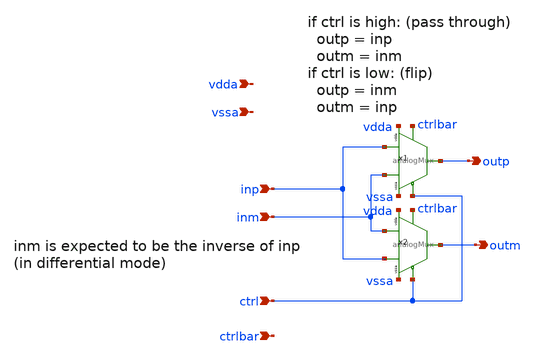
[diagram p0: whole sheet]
** sch_path: xschem/archive/mux/multiplier_differential.sch
**.subckt multiplier_differential inp inm outp outm ctrl ctrlbar vdda vssa
*.ipin inp
*.ipin inm
*.opin outp
*.opin outm
*.ipin ctrl
*.ipin ctrlbar
*.ipin vdda
*.ipin vssa
x1 inm inp ctrlbar ctrl outp vssa vdda analogMux
x2 inp inm ctrlbar ctrl outm vssa vdda analogMux
**.ends

* expanding   symbol:  mux/analogMux.sym # of pins=7
** sym_path: xschem/mux/analogMux.sym
** sch_path: xschem/mux/analogMux.sch
.subckt analogMux vref2 vref1 c cbar out vssa vdda
*.ipin vref1
*.opin out
*.ipin vref2
*.ipin c
*.ipin cbar
*.ipin vssa
*.ipin vdda
XM2 vref1 c out vssa sky130_fd_pr__nfet_01v8 L=0.15 W=0.42 nf=1 ad='int((nf+1)/2) * W/nf * 0.29' as='int((nf+2)/2) * W/nf * 0.29'
+ pd='2*int((nf+1)/2) * (W/nf + 0.29)' ps='2*int((nf+2)/2) * (W/nf + 0.29)' nrd='0.29 / W' nrs='0.29 / W'
+ sa=0 sb=0 sd=0 mult=1 m=1
XM4 vref1 cbar out vdda sky130_fd_pr__pfet_01v8 L=0.15 W=0.42 nf=1 ad='int((nf+1)/2) * W/nf * 0.29' as='int((nf+2)/2) * W/nf * 0.29'
+ pd='2*int((nf+1)/2) * (W/nf + 0.29)' ps='2*int((nf+2)/2) * (W/nf + 0.29)' nrd='0.29 / W' nrs='0.29 / W'
+ sa=0 sb=0 sd=0 mult=1 m=1
XM7 out cbar vref2 vssa sky130_fd_pr__nfet_01v8 L=0.15 W=0.42 nf=1 ad='int((nf+1)/2) * W/nf * 0.29' as='int((nf+2)/2) * W/nf * 0.29'
+ pd='2*int((nf+1)/2) * (W/nf + 0.29)' ps='2*int((nf+2)/2) * (W/nf + 0.29)' nrd='0.29 / W' nrs='0.29 / W'
+ sa=0 sb=0 sd=0 mult=1 m=1
XM8 out c vref2 vdda sky130_fd_pr__pfet_01v8 L=0.15 W=0.42 nf=1 ad='int((nf+1)/2) * W/nf * 0.29' as='int((nf+2)/2) * W/nf * 0.29'
+ pd='2*int((nf+1)/2) * (W/nf + 0.29)' ps='2*int((nf+2)/2) * (W/nf + 0.29)' nrd='0.29 / W' nrs='0.29 / W'
+ sa=0 sb=0 sd=0 mult=1 m=1
.ends

.end
